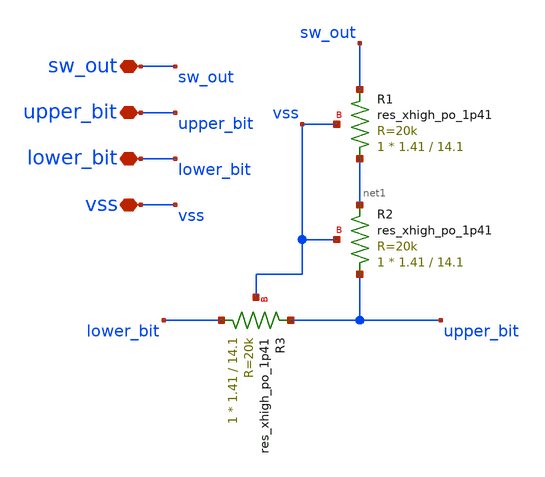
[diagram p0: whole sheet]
** sch_path: xschem/uc_res_x3/uc_res_x3.sch
**.subckt uc_res_x3 sw_out upper_bit lower_bit vss
*.iopin sw_out
*.iopin upper_bit
*.iopin lower_bit
*.iopin vss
XR1 net1 sw_out vss sky130_fd_pr__res_xhigh_po_1p41 L=14.1 mult=1 m=1
XR2 upper_bit net1 vss sky130_fd_pr__res_xhigh_po_1p41 L=14.1 mult=1 m=1
XR3 lower_bit upper_bit vss sky130_fd_pr__res_xhigh_po_1p41 L=14.1 mult=1 m=1
**.ends
.end
